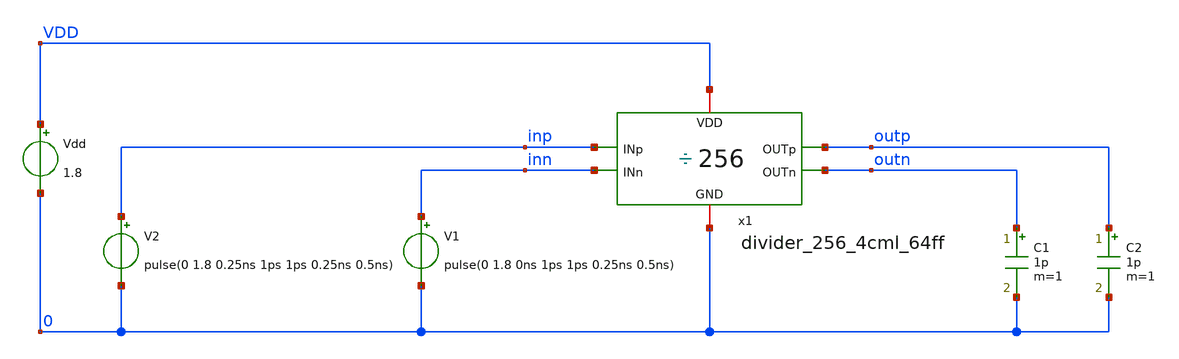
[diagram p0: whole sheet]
** sch_path: design/divider_256_4cml_64ff/tests/divider_256_4cml_64ff.sch
**.subckt divider_256_4cml_64ff
V1 inn 0 pulse(0 1.8 0ns 1ps 1ps 0.25ns 0.5ns)
Vdd VDD 0 1.8
C1 outn 0 1p m=1
V2 inp 0 pulse(0 1.8 0.25ns 1ps 1ps 0.25ns 0.5ns)
C2 outp 0 1p m=1
x1 VDD outp inp inn outn 0 divider_256_4cml_64ff
**** begin user architecture code


*.option PARHIER=LOCAL RUNLVL=6 post MODMONTE=1 warn maxwarns=400
*.option ITL4=20000 ITL5=0
* .option sampling_method = SRS
* .option method=gear

*.lib xh018/xh018.lib tm
.include 'xh018_ng/xh018.lib'

*.option rshunt = 1.0e3
*.option keepopinfo = 1

.temp 30
.tran  0.1e-9 10e-6 uic
*.dc Vdd 1.8 1.8 0.25


**** end user architecture code
**.ends
.end
